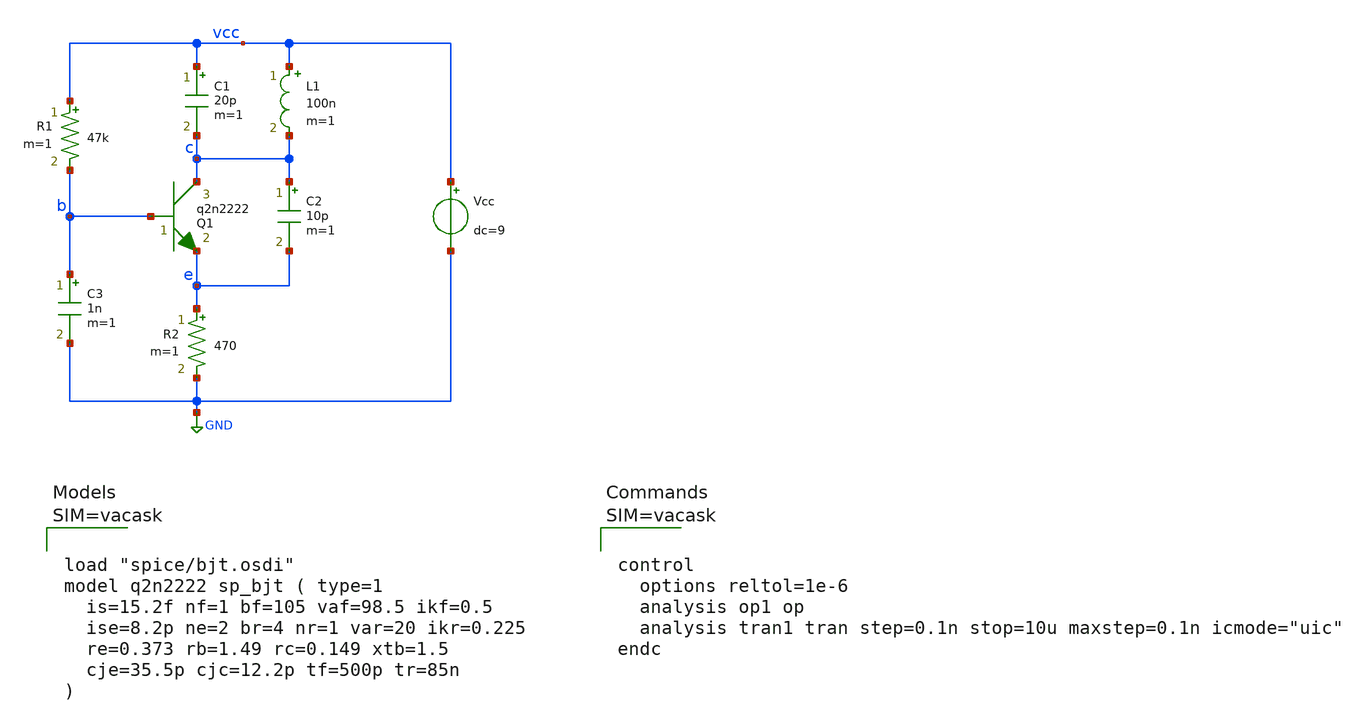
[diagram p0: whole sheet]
** sch_path: demo/xschem/rfosc.sch
**.subckt rfosc
Q1 c b e q2n2222 area=1 m=1
R1 vcc b 47k m=1
R2 e GND 470 m=1
C1 vcc c 20p m=1
C2 c e 10p m=1
C3 b GND 1n m=1
L1 vcc c 100n m=1
Vcc vcc GND dc=9
**** begin user architecture code






**** end user architecture code
**.ends
.GLOBAL GND
.end
